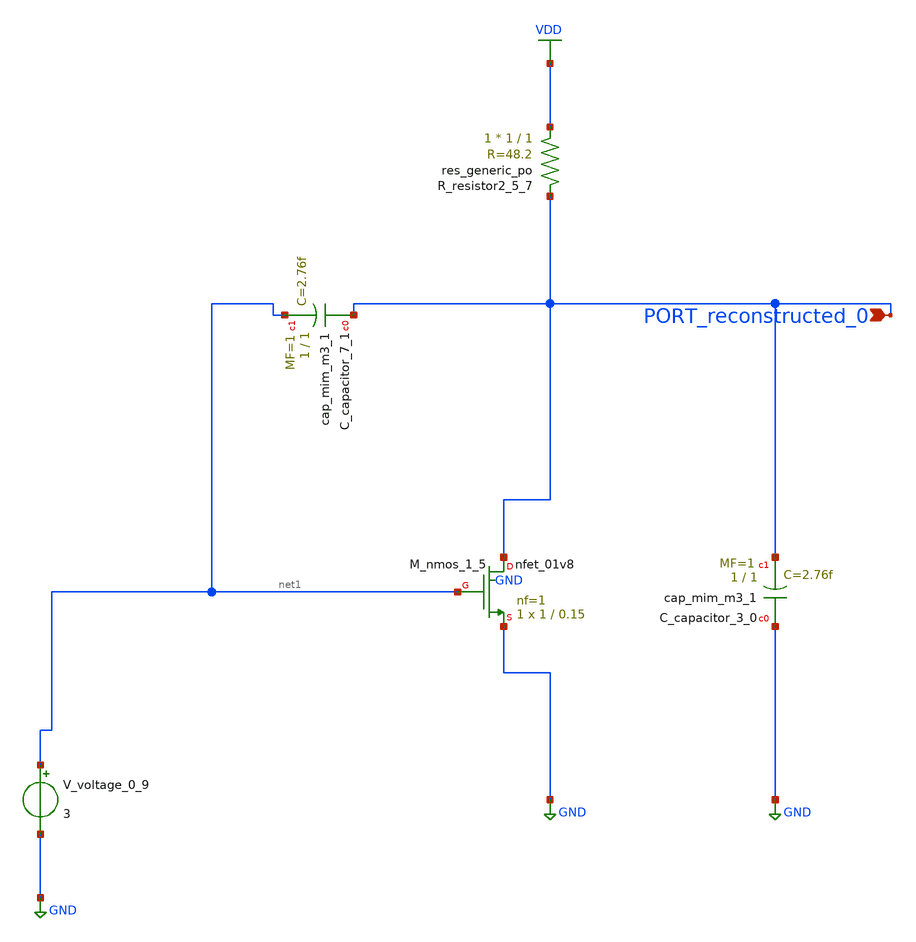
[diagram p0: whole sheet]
** sch_path: schematics/AMSNet/367.sch
**.subckt 367 PORT_reconstructed_0
*.ipin PORT_reconstructed_0
XC_capacitor_3_0 GND PORT_reconstructed_0 sky130_fd_pr__cap_mim_m3_1 W=1 L=1 MF=1 m=1
XC_capacitor_7_1 PORT_reconstructed_0 net1 sky130_fd_pr__cap_mim_m3_1 W=1 L=1 MF=1 m=1
XM_nmos_1_5 PORT_reconstructed_0 net1 GND GND sky130_fd_pr__nfet_01v8 L=0.15 W=1 nf=1 ad='int((1 + 1)/2) * 1 / 1 * 0.29'
+ as='int((1 + 2)/2) * 1 / 1 * 0.29' pd='2*int((1 + 1)/2) * (1 / 1 + 0.29)' ps='2*int((1 + 2)/2) * (1 / 1 + 0.29)'
+ nrd='0.29 / 1 ' nrs='0.29 / 1 ' sa=0 sb=0 sd=0 mult=1 m=1
XR_resistor2_5_7 VDD PORT_reconstructed_0 sky130_fd_pr__res_generic_po W=1 L=1 m=1
V_voltage_0_9 net1 GND 3
**.ends
.GLOBAL GND
.GLOBAL VDD
.end
